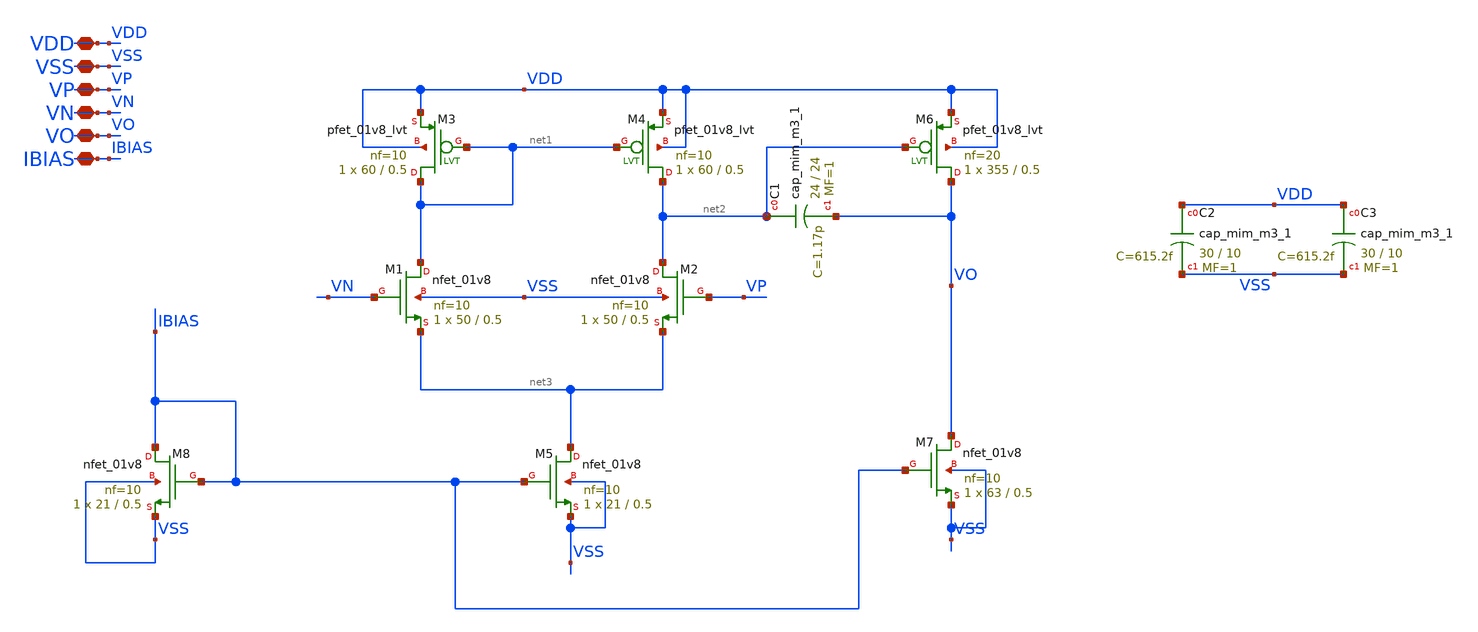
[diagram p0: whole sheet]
** sch_path: xschem/xschem_BGR_Top/Sigma_Delta/Op_Amp/OpampM.sch
**.subckt OpampM VDD VSS VP VN VO IBIAS
*.iopin VDD
*.iopin VSS
*.iopin VP
*.iopin VN
*.iopin VO
*.iopin IBIAS
XM1 net1 VN net3 VSS sky130_fd_pr__nfet_01v8 L=0.5 W=50 nf=10 ad='int((nf+1)/2) * W/nf * 0.29' as='int((nf+2)/2) * W/nf * 0.29'
+ pd='2*int((nf+1)/2) * (W/nf + 0.29)' ps='2*int((nf+2)/2) * (W/nf + 0.29)' nrd='0.29 / W' nrs='0.29 / W'
+ sa=0 sb=0 sd=0 mult=1 m=1
XM3 net1 net1 VDD VDD sky130_fd_pr__pfet_01v8_lvt L=0.5 W=60 nf=10 ad='int((nf+1)/2) * W/nf * 0.29' as='int((nf+2)/2) * W/nf * 0.29'
+ pd='2*int((nf+1)/2) * (W/nf + 0.29)' ps='2*int((nf+2)/2) * (W/nf + 0.29)' nrd='0.29 / W' nrs='0.29 / W'
+ sa=0 sb=0 sd=0 mult=1 m=1
XM2 net2 VP net3 VSS sky130_fd_pr__nfet_01v8 L=0.5 W=50 nf=10 ad='int((nf+1)/2) * W/nf * 0.29' as='int((nf+2)/2) * W/nf * 0.29'
+ pd='2*int((nf+1)/2) * (W/nf + 0.29)' ps='2*int((nf+2)/2) * (W/nf + 0.29)' nrd='0.29 / W' nrs='0.29 / W'
+ sa=0 sb=0 sd=0 mult=1 m=1
XM4 net2 net1 VDD VDD sky130_fd_pr__pfet_01v8_lvt L=0.5 W=60 nf=10 ad='int((nf+1)/2) * W/nf * 0.29' as='int((nf+2)/2) * W/nf * 0.29'
+ pd='2*int((nf+1)/2) * (W/nf + 0.29)' ps='2*int((nf+2)/2) * (W/nf + 0.29)' nrd='0.29 / W' nrs='0.29 / W'
+ sa=0 sb=0 sd=0 mult=1 m=1
XM5 net3 IBIAS VSS VSS sky130_fd_pr__nfet_01v8 L=0.5 W=21 nf=10 ad='int((nf+1)/2) * W/nf * 0.29' as='int((nf+2)/2) * W/nf * 0.29'
+ pd='2*int((nf+1)/2) * (W/nf + 0.29)' ps='2*int((nf+2)/2) * (W/nf + 0.29)' nrd='0.29 / W' nrs='0.29 / W'
+ sa=0 sb=0 sd=0 mult=1 m=1
XM6 VO net2 VDD VDD sky130_fd_pr__pfet_01v8_lvt L=0.5 W=355 nf=20 ad='int((nf+1)/2) * W/nf * 0.29' as='int((nf+2)/2) * W/nf * 0.29'
+ pd='2*int((nf+1)/2) * (W/nf + 0.29)' ps='2*int((nf+2)/2) * (W/nf + 0.29)' nrd='0.29 / W' nrs='0.29 / W'
+ sa=0 sb=0 sd=0 mult=1 m=1
XM7 VO IBIAS VSS VSS sky130_fd_pr__nfet_01v8 L=0.5 W=63 nf=10 ad='int((nf+1)/2) * W/nf * 0.29' as='int((nf+2)/2) * W/nf * 0.29'
+ pd='2*int((nf+1)/2) * (W/nf + 0.29)' ps='2*int((nf+2)/2) * (W/nf + 0.29)' nrd='0.29 / W' nrs='0.29 / W'
+ sa=0 sb=0 sd=0 mult=1 m=1
XM8 IBIAS IBIAS VSS VSS sky130_fd_pr__nfet_01v8 L=0.5 W=21 nf=10 ad='int((nf+1)/2) * W/nf * 0.29' as='int((nf+2)/2) * W/nf * 0.29'
+ pd='2*int((nf+1)/2) * (W/nf + 0.29)' ps='2*int((nf+2)/2) * (W/nf + 0.29)' nrd='0.29 / W' nrs='0.29 / W'
+ sa=0 sb=0 sd=0 mult=1 m=1
XC1 net2 VO sky130_fd_pr__cap_mim_m3_1 W=24 L=24 MF=1 m=1
XC2 VDD VSS sky130_fd_pr__cap_mim_m3_1 W=30 L=10 MF=1 m=1
XC3 VDD VSS sky130_fd_pr__cap_mim_m3_1 W=30 L=10 MF=1 m=1
**.ends
.end
